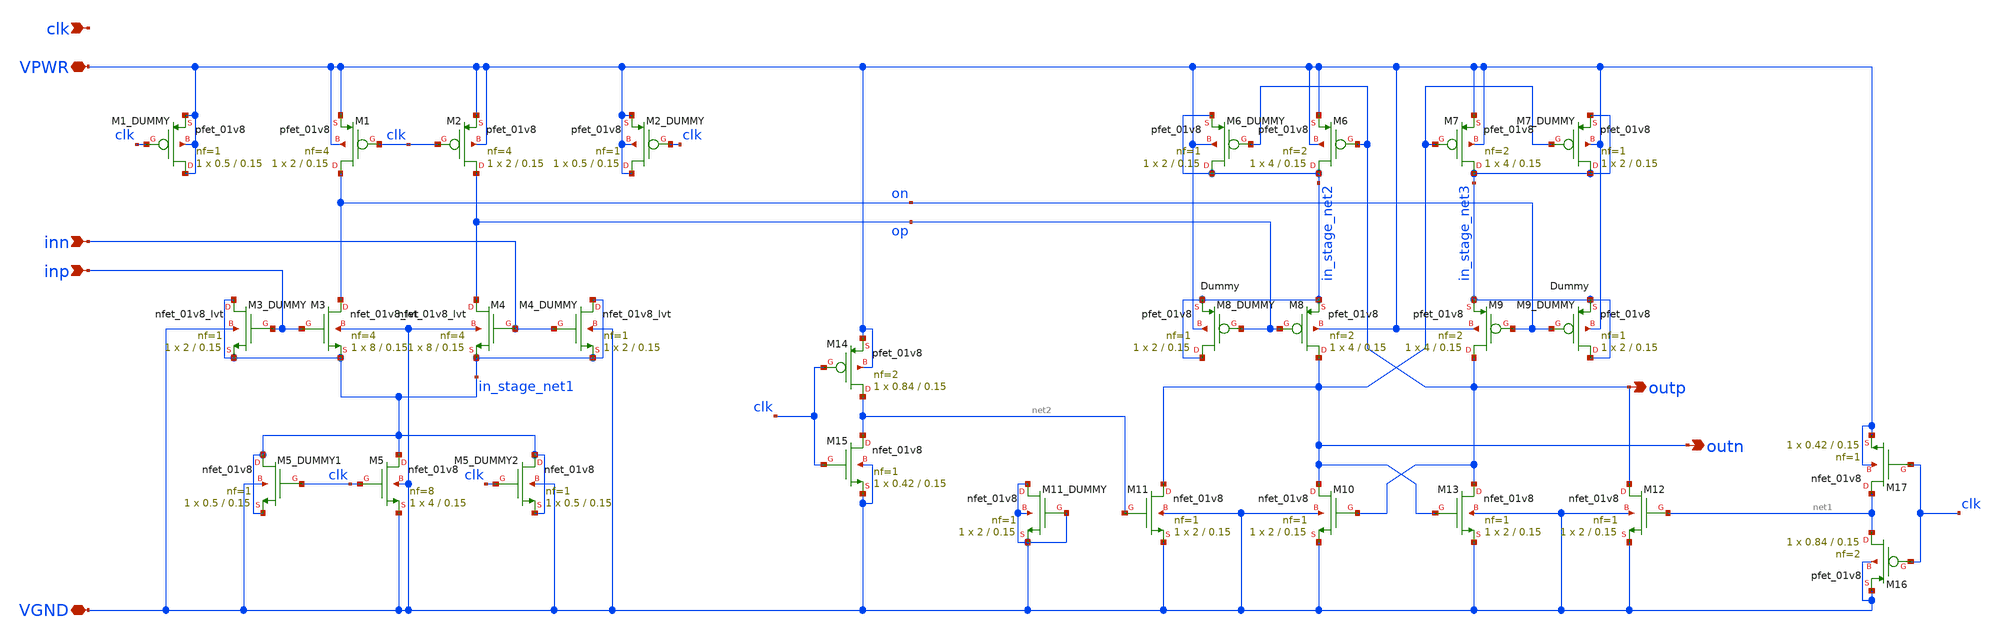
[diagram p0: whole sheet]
** sch_path: xschem/comparator.sch
**.subckt comparator VPWR VGND clk inp inn outn outp
*.iopin VPWR
*.iopin VGND
*.ipin clk
*.ipin inp
*.ipin inn
*.opin outn
*.opin outp
XM3 on inp in_stage_net1 VGND sky130_fd_pr__nfet_01v8_lvt L=0.15 W=8 nf=4 ad='int((nf+1)/2) * W/nf * 0.29'
+ as='int((nf+2)/2) * W/nf * 0.29' pd='2*int((nf+1)/2) * (W/nf + 0.29)' ps='2*int((nf+2)/2) * (W/nf + 0.29)'
+ nrd='0.29 / W' nrs='0.29 / W' sa=0 sb=0 sd=0 mult=1 m=1
XM4 op inn in_stage_net1 VGND sky130_fd_pr__nfet_01v8_lvt L=0.15 W=8 nf=4 ad='int((nf+1)/2) * W/nf * 0.29'
+ as='int((nf+2)/2) * W/nf * 0.29' pd='2*int((nf+1)/2) * (W/nf + 0.29)' ps='2*int((nf+2)/2) * (W/nf + 0.29)'
+ nrd='0.29 / W' nrs='0.29 / W' sa=0 sb=0 sd=0 mult=1 m=1
XM5 in_stage_net1 clk VGND VGND sky130_fd_pr__nfet_01v8 L=0.15 W=4 nf=8 ad='int((nf+1)/2) * W/nf * 0.29'
+ as='int((nf+2)/2) * W/nf * 0.29' pd='2*int((nf+1)/2) * (W/nf + 0.29)' ps='2*int((nf+2)/2) * (W/nf + 0.29)'
+ nrd='0.29 / W' nrs='0.29 / W' sa=0 sb=0 sd=0 mult=1 m=1
XM6 in_stage_net2 outp VPWR VPWR sky130_fd_pr__pfet_01v8 L=0.15 W=4 nf=2 ad='int((nf+1)/2) * W/nf * 0.29'
+ as='int((nf+2)/2) * W/nf * 0.29' pd='2*int((nf+1)/2) * (W/nf + 0.29)' ps='2*int((nf+2)/2) * (W/nf + 0.29)'
+ nrd='0.29 / W' nrs='0.29 / W' sa=0 sb=0 sd=0 mult=1 m=1
XM7 in_stage_net3 outn VPWR VPWR sky130_fd_pr__pfet_01v8 L=0.15 W=4 nf=2 ad='int((nf+1)/2) * W/nf * 0.29'
+ as='int((nf+2)/2) * W/nf * 0.29' pd='2*int((nf+1)/2) * (W/nf + 0.29)' ps='2*int((nf+2)/2) * (W/nf + 0.29)'
+ nrd='0.29 / W' nrs='0.29 / W' sa=0 sb=0 sd=0 mult=1 m=1
XM8 outn op in_stage_net2 VPWR sky130_fd_pr__pfet_01v8 L=0.15 W=4 nf=2 ad='int((nf+1)/2) * W/nf * 0.29'
+ as='int((nf+2)/2) * W/nf * 0.29' pd='2*int((nf+1)/2) * (W/nf + 0.29)' ps='2*int((nf+2)/2) * (W/nf + 0.29)'
+ nrd='0.29 / W' nrs='0.29 / W' sa=0 sb=0 sd=0 mult=1 m=1
XM9 outp on in_stage_net3 VPWR sky130_fd_pr__pfet_01v8 L=0.15 W=4 nf=2 ad='int((nf+1)/2) * W/nf * 0.29'
+ as='int((nf+2)/2) * W/nf * 0.29' pd='2*int((nf+1)/2) * (W/nf + 0.29)' ps='2*int((nf+2)/2) * (W/nf + 0.29)'
+ nrd='0.29 / W' nrs='0.29 / W' sa=0 sb=0 sd=0 mult=1 m=1
XM10 outn outp VGND VGND sky130_fd_pr__nfet_01v8 L=0.15 W=2 nf=1 ad='int((nf+1)/2) * W/nf * 0.29' as='int((nf+2)/2) * W/nf * 0.29'
+ pd='2*int((nf+1)/2) * (W/nf + 0.29)' ps='2*int((nf+2)/2) * (W/nf + 0.29)' nrd='0.29 / W' nrs='0.29 / W'
+ sa=0 sb=0 sd=0 mult=1 m=1
XM11 outn net2 VGND VGND sky130_fd_pr__nfet_01v8 L=0.15 W=2 nf=1 ad='int((nf+1)/2) * W/nf * 0.29' as='int((nf+2)/2) * W/nf * 0.29'
+ pd='2*int((nf+1)/2) * (W/nf + 0.29)' ps='2*int((nf+2)/2) * (W/nf + 0.29)' nrd='0.29 / W' nrs='0.29 / W'
+ sa=0 sb=0 sd=0 mult=1 m=1
XM12 outp net1 VGND VGND sky130_fd_pr__nfet_01v8 L=0.15 W=2 nf=1 ad='int((nf+1)/2) * W/nf * 0.29' as='int((nf+2)/2) * W/nf * 0.29'
+ pd='2*int((nf+1)/2) * (W/nf + 0.29)' ps='2*int((nf+2)/2) * (W/nf + 0.29)' nrd='0.29 / W' nrs='0.29 / W'
+ sa=0 sb=0 sd=0 mult=1 m=1
XM13 outp outn VGND VGND sky130_fd_pr__nfet_01v8 L=0.15 W=2 nf=1 ad='int((nf+1)/2) * W/nf * 0.29' as='int((nf+2)/2) * W/nf * 0.29'
+ pd='2*int((nf+1)/2) * (W/nf + 0.29)' ps='2*int((nf+2)/2) * (W/nf + 0.29)' nrd='0.29 / W' nrs='0.29 / W'
+ sa=0 sb=0 sd=0 mult=1 m=1
XM2 op clk VPWR VPWR sky130_fd_pr__pfet_01v8 L=0.15 W=2 nf=4 ad='int((nf+1)/2) * W/nf * 0.29' as='int((nf+2)/2) * W/nf * 0.29'
+ pd='2*int((nf+1)/2) * (W/nf + 0.29)' ps='2*int((nf+2)/2) * (W/nf + 0.29)' nrd='0.29 / W' nrs='0.29 / W'
+ sa=0 sb=0 sd=0 mult=1 m=1
XM1 on clk VPWR VPWR sky130_fd_pr__pfet_01v8 L=0.15 W=2 nf=4 ad='int((nf+1)/2) * W/nf * 0.29' as='int((nf+2)/2) * W/nf * 0.29'
+ pd='2*int((nf+1)/2) * (W/nf + 0.29)' ps='2*int((nf+2)/2) * (W/nf + 0.29)' nrd='0.29 / W' nrs='0.29 / W'
+ sa=0 sb=0 sd=0 mult=1 m=1
XM4_DUMMY in_stage_net1 inn in_stage_net1 VGND sky130_fd_pr__nfet_01v8_lvt L=0.15 W=2 nf=1 ad='int((nf+1)/2) * W/nf * 0.29'
+ as='int((nf+2)/2) * W/nf * 0.29' pd='2*int((nf+1)/2) * (W/nf + 0.29)' ps='2*int((nf+2)/2) * (W/nf + 0.29)'
+ nrd='0.29 / W' nrs='0.29 / W' sa=0 sb=0 sd=0 mult=1 m=1
XM3_DUMMY in_stage_net1 inp in_stage_net1 VGND sky130_fd_pr__nfet_01v8_lvt L=0.15 W=2 nf=1 ad='int((nf+1)/2) * W/nf * 0.29'
+ as='int((nf+2)/2) * W/nf * 0.29' pd='2*int((nf+1)/2) * (W/nf + 0.29)' ps='2*int((nf+2)/2) * (W/nf + 0.29)'
+ nrd='0.29 / W' nrs='0.29 / W' sa=0 sb=0 sd=0 mult=1 m=1
XM5_DUMMY2 in_stage_net1 clk in_stage_net1 VGND sky130_fd_pr__nfet_01v8 L=0.15 W=0.5 nf=1 ad='int((nf+1)/2) * W/nf * 0.29'
+ as='int((nf+2)/2) * W/nf * 0.29' pd='2*int((nf+1)/2) * (W/nf + 0.29)' ps='2*int((nf+2)/2) * (W/nf + 0.29)'
+ nrd='0.29 / W' nrs='0.29 / W' sa=0 sb=0 sd=0 mult=1 m=1
XM5_DUMMY1 in_stage_net1 clk in_stage_net1 VGND sky130_fd_pr__nfet_01v8 L=0.15 W=0.5 nf=1 ad='int((nf+1)/2) * W/nf * 0.29'
+ as='int((nf+2)/2) * W/nf * 0.29' pd='2*int((nf+1)/2) * (W/nf + 0.29)' ps='2*int((nf+2)/2) * (W/nf + 0.29)'
+ nrd='0.29 / W' nrs='0.29 / W' sa=0 sb=0 sd=0 mult=1 m=1
XM2_DUMMY VPWR clk VPWR VPWR sky130_fd_pr__pfet_01v8 L=0.15 W=0.5 nf=1 ad='int((nf+1)/2) * W/nf * 0.29'
+ as='int((nf+2)/2) * W/nf * 0.29' pd='2*int((nf+1)/2) * (W/nf + 0.29)' ps='2*int((nf+2)/2) * (W/nf + 0.29)'
+ nrd='0.29 / W' nrs='0.29 / W' sa=0 sb=0 sd=0 mult=1 m=1
XM1_DUMMY VPWR clk VPWR VPWR sky130_fd_pr__pfet_01v8 L=0.15 W=0.5 nf=1 ad='int((nf+1)/2) * W/nf * 0.29'
+ as='int((nf+2)/2) * W/nf * 0.29' pd='2*int((nf+1)/2) * (W/nf + 0.29)' ps='2*int((nf+2)/2) * (W/nf + 0.29)'
+ nrd='0.29 / W' nrs='0.29 / W' sa=0 sb=0 sd=0 mult=1 m=1
XM8_DUMMY in_stage_net2 op in_stage_net2 VPWR sky130_fd_pr__pfet_01v8 L=0.15 W=2 nf=1 ad='int((nf+1)/2) * W/nf * 0.29'
+ as='int((nf+2)/2) * W/nf * 0.29' pd='2*int((nf+1)/2) * (W/nf + 0.29)' ps='2*int((nf+2)/2) * (W/nf + 0.29)'
+ nrd='0.29 / W' nrs='0.29 / W' sa=0 sb=0 sd=0 mult=1 m=1
XM9_DUMMY in_stage_net3 on in_stage_net3 VPWR sky130_fd_pr__pfet_01v8 L=0.15 W=2 nf=1 ad='int((nf+1)/2) * W/nf * 0.29'
+ as='int((nf+2)/2) * W/nf * 0.29' pd='2*int((nf+1)/2) * (W/nf + 0.29)' ps='2*int((nf+2)/2) * (W/nf + 0.29)'
+ nrd='0.29 / W' nrs='0.29 / W' sa=0 sb=0 sd=0 mult=1 m=1
XM6_DUMMY in_stage_net2 outp in_stage_net2 VPWR sky130_fd_pr__pfet_01v8 L=0.15 W=2 nf=1 ad='int((nf+1)/2) * W/nf * 0.29'
+ as='int((nf+2)/2) * W/nf * 0.29' pd='2*int((nf+1)/2) * (W/nf + 0.29)' ps='2*int((nf+2)/2) * (W/nf + 0.29)'
+ nrd='0.29 / W' nrs='0.29 / W' sa=0 sb=0 sd=0 mult=1 m=1
XM7_DUMMY in_stage_net3 outn in_stage_net3 VPWR sky130_fd_pr__pfet_01v8 L=0.15 W=2 nf=1 ad='int((nf+1)/2) * W/nf * 0.29'
+ as='int((nf+2)/2) * W/nf * 0.29' pd='2*int((nf+1)/2) * (W/nf + 0.29)' ps='2*int((nf+2)/2) * (W/nf + 0.29)'
+ nrd='0.29 / W' nrs='0.29 / W' sa=0 sb=0 sd=0 mult=1 m=1
XM11_DUMMY VGND VGND VGND VGND sky130_fd_pr__nfet_01v8 L=0.15 W=2 nf=1 ad='int((nf+1)/2) * W/nf * 0.29'
+ as='int((nf+2)/2) * W/nf * 0.29' pd='2*int((nf+1)/2) * (W/nf + 0.29)' ps='2*int((nf+2)/2) * (W/nf + 0.29)'
+ nrd='0.29 / W' nrs='0.29 / W' sa=0 sb=0 sd=0 mult=1 m=1
XM14 net2 clk VPWR VPWR sky130_fd_pr__pfet_01v8 L=0.15 W=0.84 nf=2 ad='int((nf+1)/2) * W/nf * 0.29' as='int((nf+2)/2) * W/nf * 0.29'
+ pd='2*int((nf+1)/2) * (W/nf + 0.29)' ps='2*int((nf+2)/2) * (W/nf + 0.29)' nrd='0.29 / W' nrs='0.29 / W'
+ sa=0 sb=0 sd=0 mult=1 m=1
XM15 net2 clk VGND VGND sky130_fd_pr__nfet_01v8 L=0.15 W=0.42 nf=1 ad='int((nf+1)/2) * W/nf * 0.29' as='int((nf+2)/2) * W/nf * 0.29'
+ pd='2*int((nf+1)/2) * (W/nf + 0.29)' ps='2*int((nf+2)/2) * (W/nf + 0.29)' nrd='0.29 / W' nrs='0.29 / W'
+ sa=0 sb=0 sd=0 mult=1 m=1
XM16 net1 clk VGND VGND sky130_fd_pr__pfet_01v8 L=0.15 W=0.84 nf=2 ad='int((nf+1)/2) * W/nf * 0.29' as='int((nf+2)/2) * W/nf * 0.29'
+ pd='2*int((nf+1)/2) * (W/nf + 0.29)' ps='2*int((nf+2)/2) * (W/nf + 0.29)' nrd='0.29 / W' nrs='0.29 / W'
+ sa=0 sb=0 sd=0 mult=1 m=1
XM17 net1 clk VPWR VPWR sky130_fd_pr__nfet_01v8 L=0.15 W=0.42 nf=1 ad='int((nf+1)/2) * W/nf * 0.29' as='int((nf+2)/2) * W/nf * 0.29'
+ pd='2*int((nf+1)/2) * (W/nf + 0.29)' ps='2*int((nf+2)/2) * (W/nf + 0.29)' nrd='0.29 / W' nrs='0.29 / W'
+ sa=0 sb=0 sd=0 mult=1 m=1
**.ends
.end
